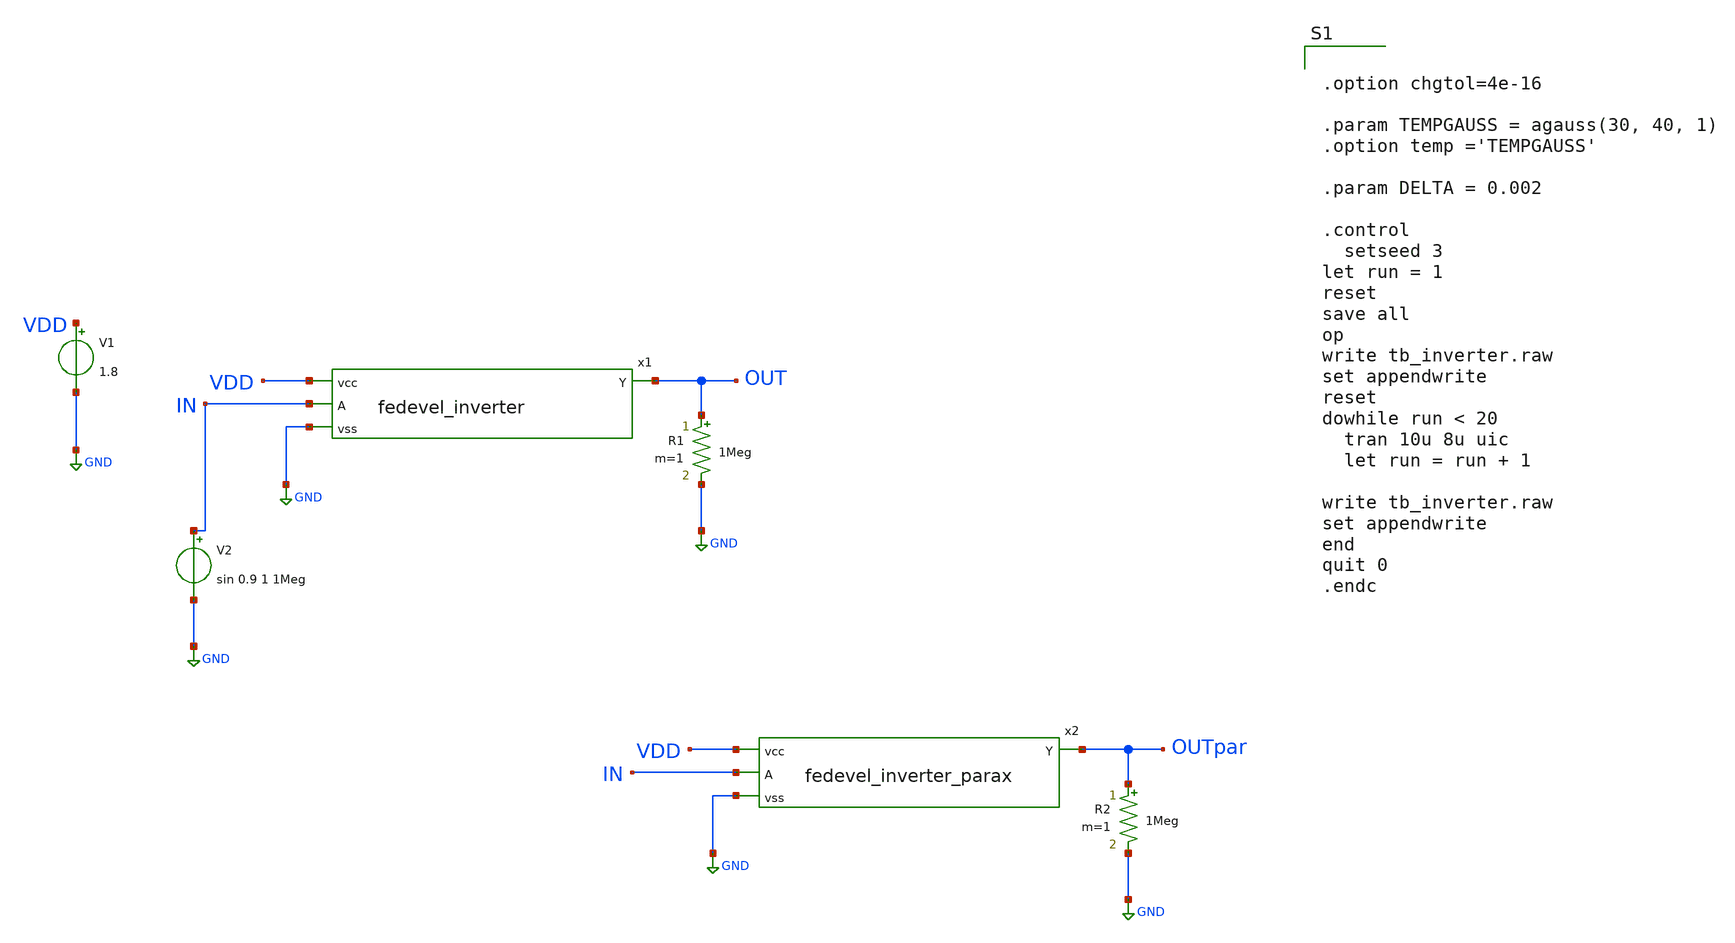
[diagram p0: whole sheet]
** sch_path: tb_inverter.sch
**.subckt tb_inverter
x1 VDD OUT IN GND fedevel_inverter
V1 VDD GND 1.8
V2 IN GND sin 0.9 1 1Meg
R1 OUT GND 1Meg m=1
x2 VDD OUTpar IN GND fedevel_inverter_parax
R2 OUTpar GND 1Meg m=1
**** begin user architecture code


.option chgtol=4e-16

.param TEMPGAUSS = agauss(30, 40, 1)
.option temp ='TEMPGAUSS'

.param DELTA = 0.002

.control
  setseed 3
let run = 1
reset
save all
op
write tb_inverter.raw
set appendwrite
reset
dowhile run < 20
  tran 10u 8u uic
  let run = run + 1

write tb_inverter.raw
set appendwrite
end
quit 0
.endc

.lib $::SKYWATER_MODELS/sky130.lib.spice tt
**** end user architecture code
**.ends

* expanding   symbol:  fedevel_inverter.sym # of pins=4
** sym_path: fedevel_inverter.sym
** sch_path: fedevel_inverter.sch
.subckt fedevel_inverter vcc Y A vss
*.ipin A
*.ipin vss
*.ipin vcc
*.opin Y
XM1 Y A vss vss sky130_fd_pr__nfet_01v8_lvt L=0.15 W=1 nf=1 ad='int((nf+1)/2) * W/nf * 0.29' as='int((nf+2)/2) * W/nf * 0.29'
+ pd='2*int((nf+1)/2) * (W/nf + 0.29)' ps='2*int((nf+2)/2) * (W/nf + 0.29)' nrd='0.29 / W' nrs='0.29 / W'
+ sa=0 sb=0 sd=0 mult=1 m=1
XM2 Y A vcc vcc sky130_fd_pr__pfet_01v8_lvt L=0.35 W=1 nf=1 ad='int((nf+1)/2) * W/nf * 0.29' as='int((nf+2)/2) * W/nf * 0.29'
+ pd='2*int((nf+1)/2) * (W/nf + 0.29)' ps='2*int((nf+2)/2) * (W/nf + 0.29)' nrd='0.29 / W' nrs='0.29 / W'
+ sa=0 sb=0 sd=0 mult=1 m=1
.ends


* expanding   symbol:  fedevel_inverter_parax.sym # of pins=4
** sym_path: fedevel_inverter.sym
.include [file normalize fedevel_inverter_parax.spice]
.GLOBAL GND
.end
